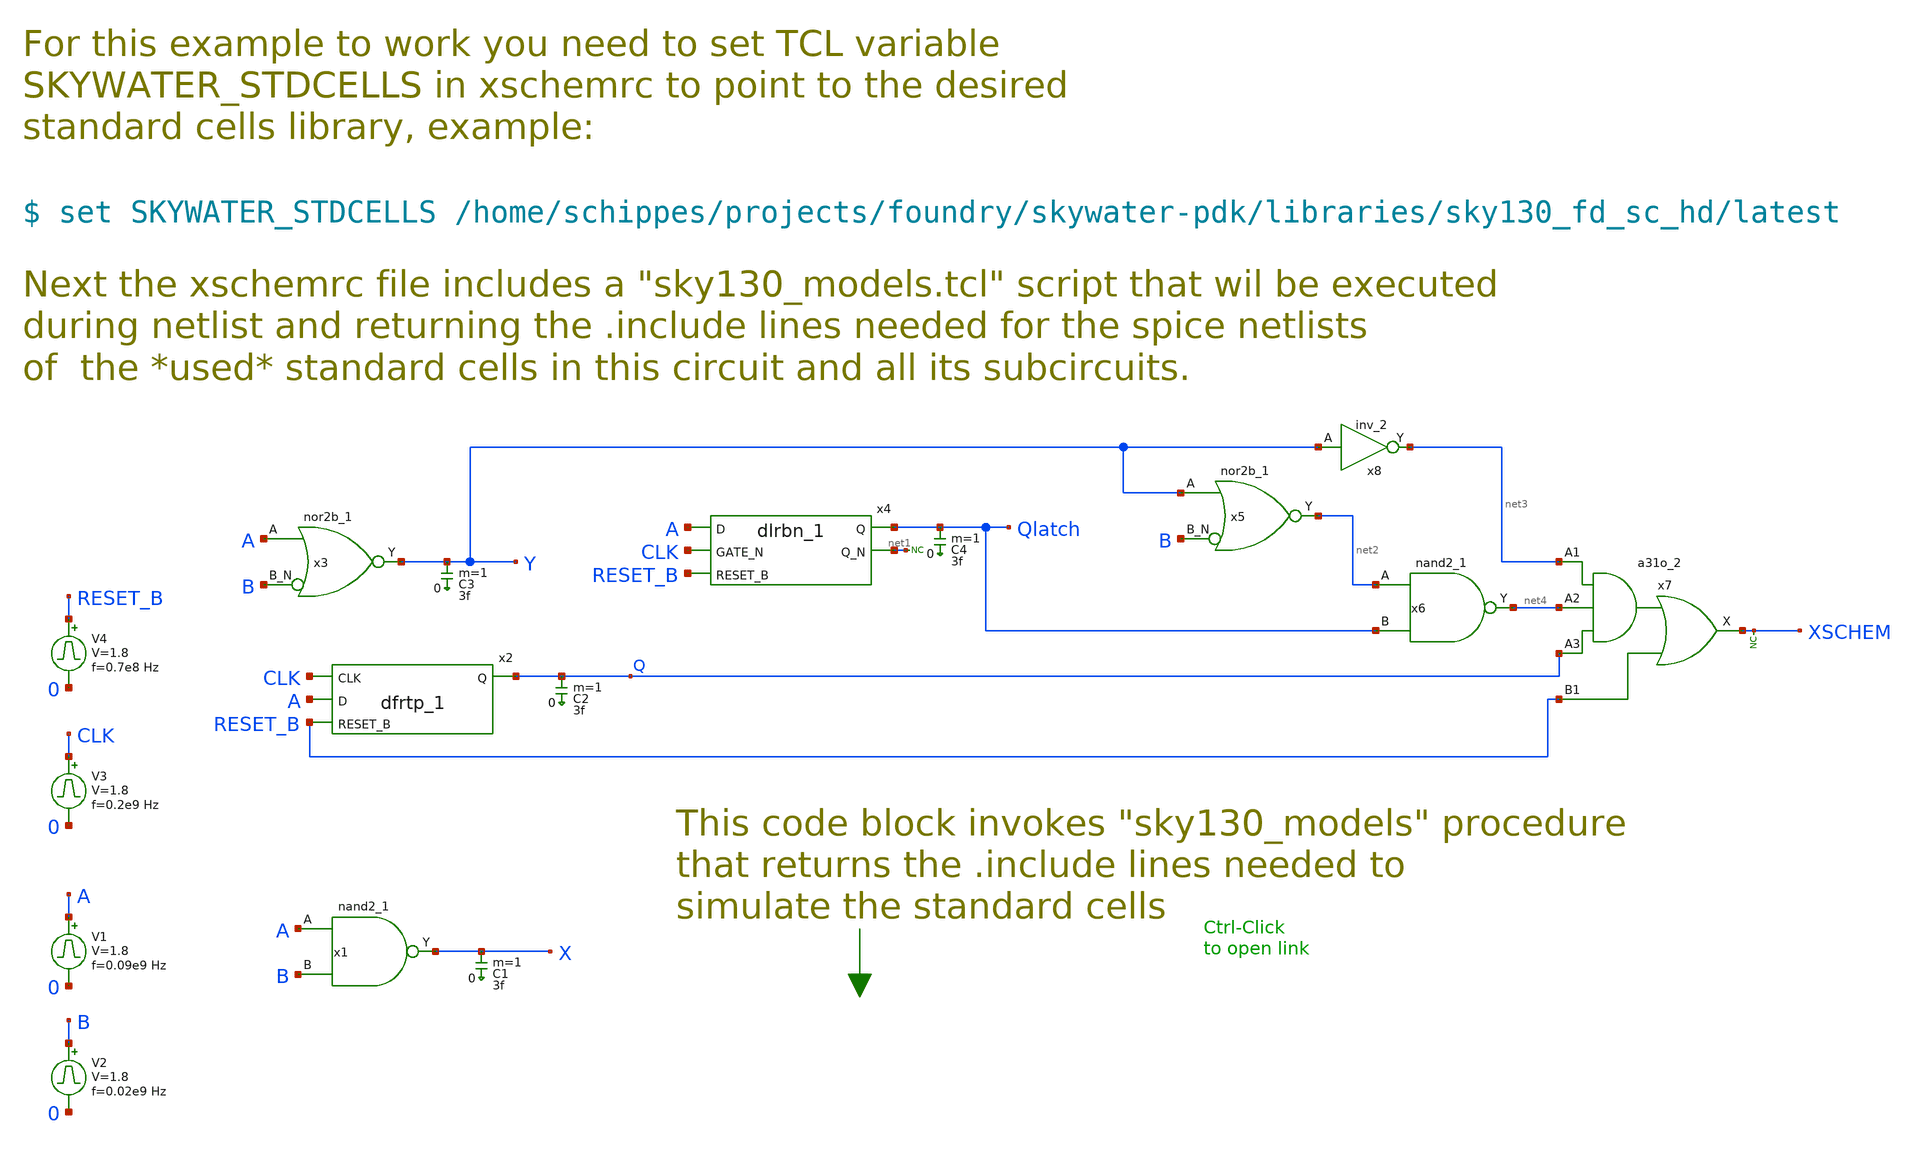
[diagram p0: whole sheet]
** sch_path: xyce/sky130A-xyce/libs.tech/xschem/sky130_tests/test_stdcells.sch
* Copyright 2020 Stefan Frederik Schippers
* Licensed under the Apache License, Version 2.0 (the "License");
* you may not use this file except in compliance with the License.
* You may obtain a copy of the License at
* https://www.apache.org/licenses/LICENSE-2.0
* Unless required by applicable law or agreed to in writing, software
* distributed under the License is distributed on an "AS IS" BASIS,
* WITHOUT WARRANTIES OR CONDITIONS OF ANY KIND, either express or implied.
* See the License for the specific language governing permissions and
* limitations under the License.
**.subckt test_stdcells
x1 A B VSS VSS VCC VCC X sky130_fd_sc_hd__nand2_1
V1 A 0 pulse 0 1.8 '0.495/ 0.09e9 ' '0.01/0.09e9 ' '0.01/0.09e9 ' '0.49/0.09e9 ' '1/0.09e9 '
V2 B 0 pulse 0 1.8 '0.495/ 0.02e9 ' '0.01/0.02e9 ' '0.01/0.02e9 ' '0.49/0.02e9 ' '1/0.02e9 '
C1 X 0 3f m=1
x2 CLK A RESET_B VSS VSS VCC VCC Q sky130_fd_sc_hd__dfrtp_1
V3 CLK 0 pulse 0 1.8 '0.495/ 0.2e9 ' '0.01/0.2e9 ' '0.01/0.2e9 ' '0.49/0.2e9 ' '1/0.2e9 '
V4 RESET_B 0 pulse 0 1.8 '0.495/ 0.7e8 ' '0.01/0.7e8 ' '0.01/0.7e8 ' '0.49/0.7e8 ' '1/0.7e8 '
C2 Q 0 3f m=1
C3 Y 0 3f m=1
x3 A B VSS VSS VCC VCC Y sky130_fd_sc_hd__nor2b_1
x4 A CLK RESET_B VSS VSS VCC VCC Qlatch net1 sky130_fd_sc_hd__dlrbn_1
C4 Qlatch 0 3f m=1
x5 Y B VSS VSS VCC VCC net2 sky130_fd_sc_hd__nor2b_1
x6 net2 Qlatch VSS VSS VCC VCC net4 sky130_fd_sc_hd__nand2_1
x7 net3 net4 Q RESET_B VSS VSS VCC VCC XSCHEM sky130_fd_sc_hd__a31o_2
* noconn #net1
* noconn XSCHEM
x8 Y VGND VNB VPB VPWR net3 sky130_fd_sc_hd__inv_2
**** begin user architecture code


.temp 25
vvcc vcc 0 dc 1.8
vvss vss 0 0
.control
tran 30p 80n
plot a b+2 clk+4 reset_b+6 x+8 y+10 q+12 qlatch+14
.endc



.include $::SKYWATER_MODELS/cells/nfet_01v8/sky130_fd_pr__nfet_01v8__tt.corner.spice
.include $::SKYWATER_MODELS/cells/nfet_01v8_lvt/sky130_fd_pr__nfet_01v8_lvt__tt.corner.spice
.include $::SKYWATER_MODELS/cells/pfet_01v8/sky130_fd_pr__pfet_01v8__tt.corner.spice
.include $::SKYWATER_MODELS/cells/nfet_03v3_nvt/sky130_fd_pr__nfet_03v3_nvt__tt.corner.spice
.include $::SKYWATER_MODELS/cells/nfet_05v0_nvt/sky130_fd_pr__nfet_05v0_nvt__tt.corner.spice
.include $::SKYWATER_MODELS/cells/esd_nfet_01v8/sky130_fd_pr__esd_nfet_01v8__tt.corner.spice
.include $::SKYWATER_MODELS/cells/pfet_01v8_lvt/sky130_fd_pr__pfet_01v8_lvt__tt.corner.spice
.include $::SKYWATER_MODELS/cells/pfet_01v8_hvt/sky130_fd_pr__pfet_01v8_hvt__tt.corner.spice
.include $::SKYWATER_MODELS/cells/esd_pfet_g5v0d10v5/sky130_fd_pr__esd_pfet_g5v0d10v5__tt.corner.spice
.include $::SKYWATER_MODELS/cells/pfet_g5v0d10v5/sky130_fd_pr__pfet_g5v0d10v5__tt.corner.spice
.include $::SKYWATER_MODELS/cells/pfet_g5v0d16v0/sky130_fd_pr__pfet_g5v0d16v0__tt.corner.spice
.include $::SKYWATER_MODELS/cells/nfet_g5v0d10v5/sky130_fd_pr__nfet_g5v0d10v5__tt.corner.spice
.include $::SKYWATER_MODELS/cells/nfet_g5v0d16v0/sky130_fd_pr__nfet_g5v0d16v0__tt_discrete.corner.spice
.include $::SKYWATER_MODELS/cells/esd_nfet_g5v0d10v5/sky130_fd_pr__esd_nfet_g5v0d10v5__tt.corner.spice
.include $::SKYWATER_MODELS/models/corners/tt/nonfet.spice
* Mismatch parameters
.include $::SKYWATER_MODELS/cells/nfet_01v8/sky130_fd_pr__nfet_01v8__mismatch.corner.spice
.include $::SKYWATER_MODELS/cells/pfet_01v8/sky130_fd_pr__pfet_01v8__mismatch.corner.spice
.include $::SKYWATER_MODELS/cells/nfet_01v8_lvt/sky130_fd_pr__nfet_01v8_lvt__mismatch.corner.spice
.include $::SKYWATER_MODELS/cells/pfet_01v8_lvt/sky130_fd_pr__pfet_01v8_lvt__mismatch.corner.spice
.include $::SKYWATER_MODELS/cells/pfet_01v8_hvt/sky130_fd_pr__pfet_01v8_hvt__mismatch.corner.spice
.include $::SKYWATER_MODELS/cells/nfet_g5v0d10v5/sky130_fd_pr__nfet_g5v0d10v5__mismatch.corner.spice
.include $::SKYWATER_MODELS/cells/pfet_g5v0d10v5/sky130_fd_pr__pfet_g5v0d10v5__mismatch.corner.spice
.include $::SKYWATER_MODELS/cells/nfet_05v0_nvt/sky130_fd_pr__nfet_05v0_nvt__mismatch.corner.spice
.include $::SKYWATER_MODELS/cells/nfet_03v3_nvt/sky130_fd_pr__nfet_03v3_nvt__mismatch.corner.spice
* Resistor$::SKYWATER_MODELS/Capacitor
.include $::SKYWATER_MODELS/models/r+c/res_typical__cap_typical.spice
.include $::SKYWATER_MODELS/models/r+c/res_typical__cap_typical__lin.spice
* Special cells
.include $::SKYWATER_MODELS/models/corners/tt/specialized_cells.spice
* All models
.include $::SKYWATER_MODELS/models/all.spice
* Corner
.include $::SKYWATER_MODELS/models/corners/tt/rf.spice

**** end user architecture code
**.ends
**** begin user architecture code
[sky130_models]
**** end user architecture code
.end
